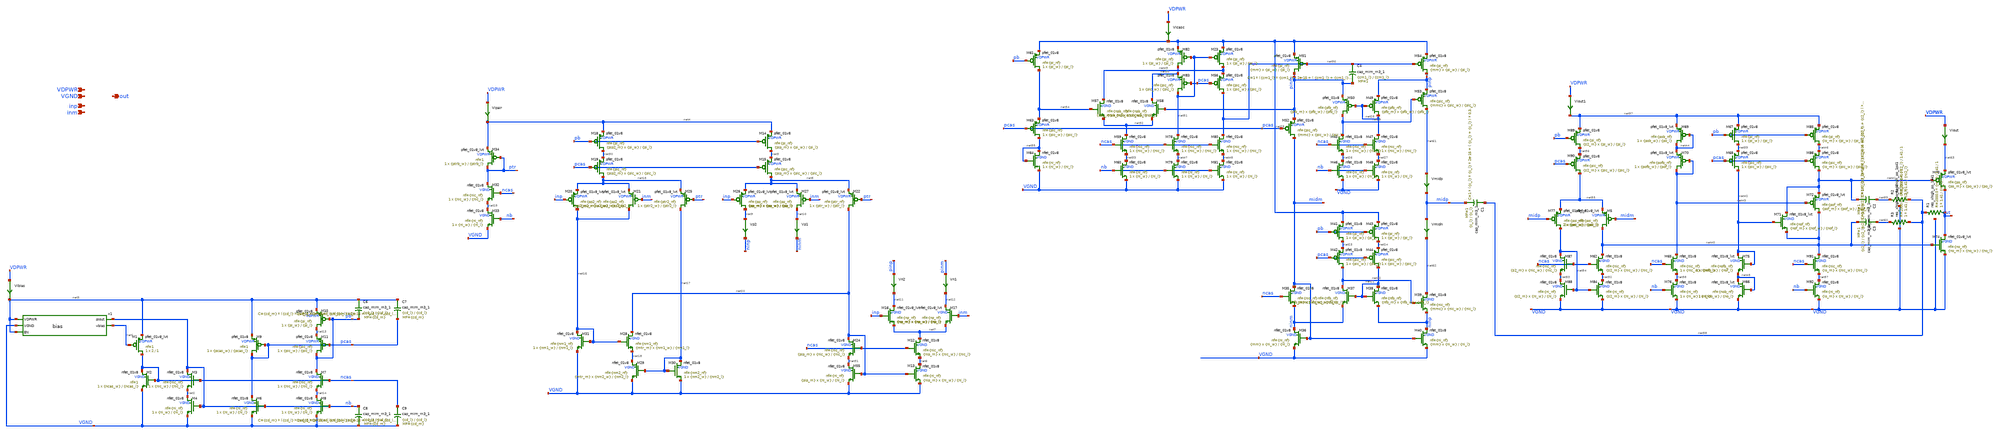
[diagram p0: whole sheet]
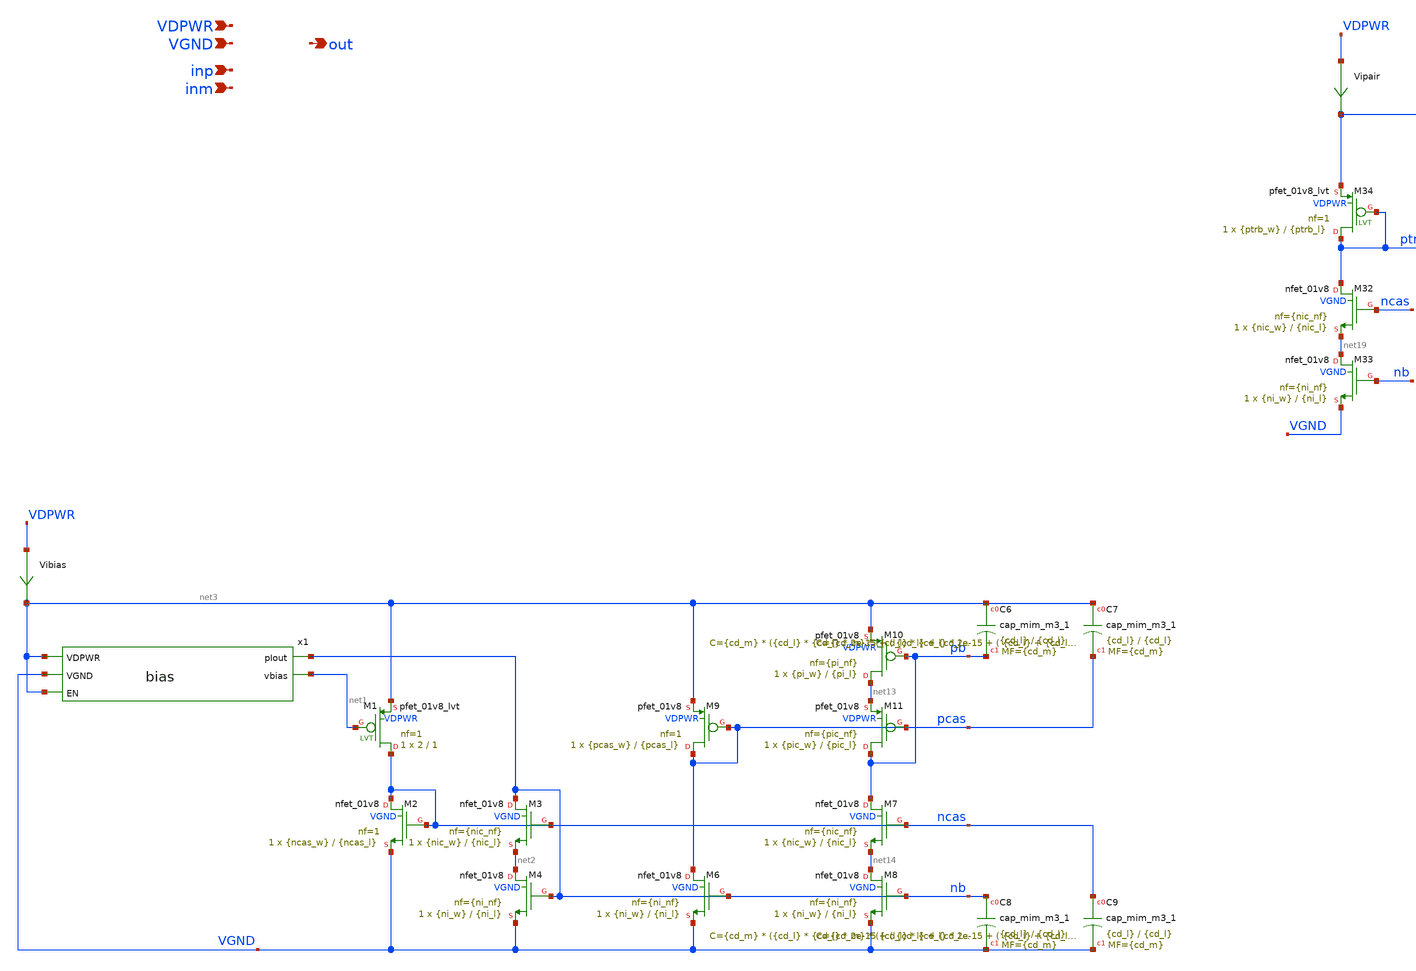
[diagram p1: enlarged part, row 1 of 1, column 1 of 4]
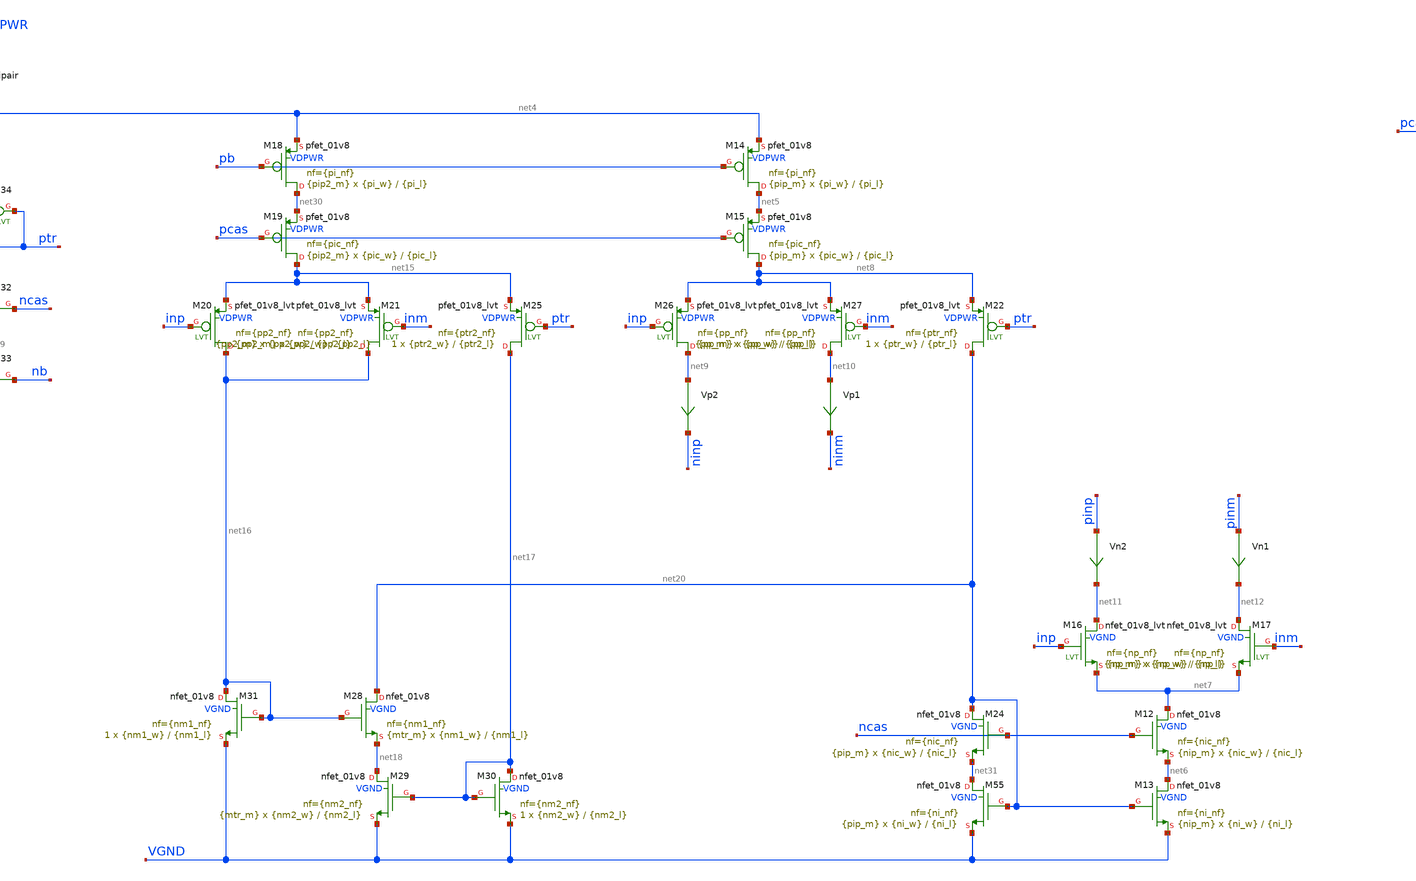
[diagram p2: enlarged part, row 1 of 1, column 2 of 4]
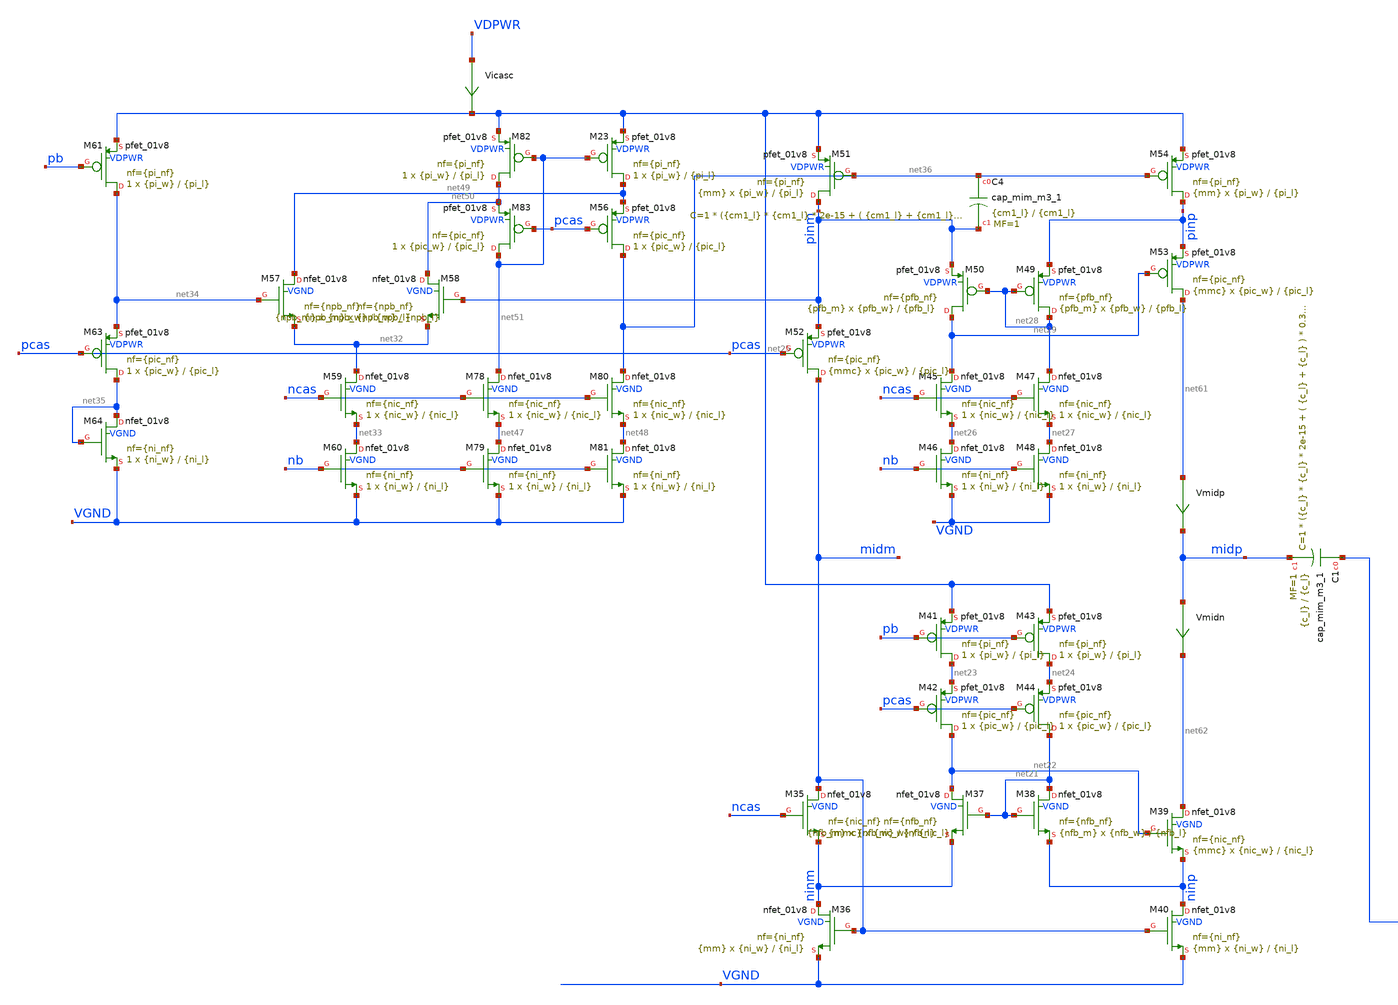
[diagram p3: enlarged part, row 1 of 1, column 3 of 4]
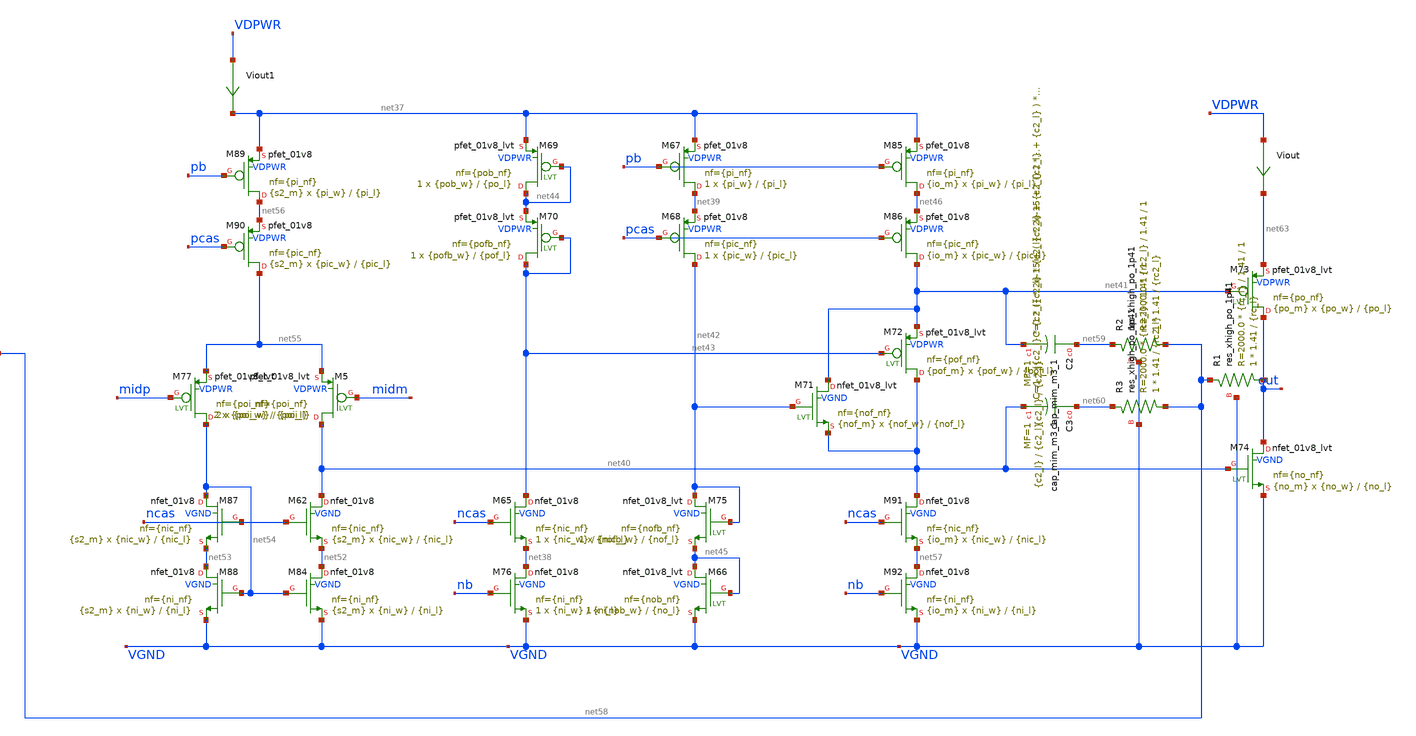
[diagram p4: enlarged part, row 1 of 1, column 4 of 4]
** sch_path: xschem/opamp_testing2.sch
**.subckt opamp_testing2 VDPWR VGND inp inm out
*.ipin VDPWR
*.ipin VGND
*.ipin inp
*.ipin inm
*.opin out
x1 net3 nb VGND net3 net1 bias
XM1 ncas net1 net3 VDPWR sky130_fd_pr__pfet_01v8_lvt L=1 W=2 nf=1 ad='int((1 + 1)/2) * 2 / 1 * 0.29'
+ as='int((1 + 2)/2) * 2 / 1 * 0.29' pd='2*int((1 + 1)/2) * (2 / 1 + 0.29)' ps='2*int((1 + 2)/2) * (2 / 1 + 0.29)'
+ nrd='0.29 / 2 ' nrs='0.29 / 2 ' sa=0 sb=0 sd=0 mult=1 m=1
XM2 ncas ncas VGND VGND sky130_fd_pr__nfet_01v8 L={ncas_l} W={ncas_w} nf=1 ad='int((1 + 1)/2) * {ncas_w} / 1 * 0.29'
+ as='int((1 + 2)/2) * {ncas_w} / 1 * 0.29' pd='2*int((1 + 1)/2) * ({ncas_w} / 1 + 0.29)' ps='2*int((1 + 2)/2) * ({ncas_w} / 1 + 0.29)'
+ nrd='0.29 / {ncas_w} ' nrs='0.29 / {ncas_w} ' sa=0 sb=0 sd=0 mult=1 m=1
XM3 nb ncas net2 VGND sky130_fd_pr__nfet_01v8 L={nic_l} W={nic_w} nf={nic_nf} ad='int(({nic_nf} + 1)/2) * {nic_w} / {nic_nf} * 0.29'
+ as='int(({nic_nf} + 2)/2) * {nic_w} / {nic_nf} * 0.29' pd='2*int(({nic_nf} + 1)/2) * ({nic_w} / {nic_nf} + 0.29)'
+ ps='2*int(({nic_nf} + 2)/2) * ({nic_w} / {nic_nf} + 0.29)' nrd='0.29 / {nic_w} ' nrs='0.29 / {nic_w} '
+ sa=0 sb=0 sd=0 mult=1 m=1
XM4 net2 nb VGND VGND sky130_fd_pr__nfet_01v8 L={ni_l} W={ni_w} nf={ni_nf} ad='int(({ni_nf} + 1)/2) * {ni_w} / {ni_nf} * 0.29'
+ as='int(({ni_nf} + 2)/2) * {ni_w} / {ni_nf} * 0.29' pd='2*int(({ni_nf} + 1)/2) * ({ni_w} / {ni_nf} + 0.29)'
+ ps='2*int(({ni_nf} + 2)/2) * ({ni_w} / {ni_nf} + 0.29)' nrd='0.29 / {ni_w} ' nrs='0.29 / {ni_w} ' sa=0
+ sb=0 sd=0 mult=1 m=1
XM6 pcas nb VGND VGND sky130_fd_pr__nfet_01v8 L={ni_l} W={ni_w} nf={ni_nf} ad='int(({ni_nf} + 1)/2) * {ni_w} / {ni_nf} * 0.29'
+ as='int(({ni_nf} + 2)/2) * {ni_w} / {ni_nf} * 0.29' pd='2*int(({ni_nf} + 1)/2) * ({ni_w} / {ni_nf} + 0.29)'
+ ps='2*int(({ni_nf} + 2)/2) * ({ni_w} / {ni_nf} + 0.29)' nrd='0.29 / {ni_w} ' nrs='0.29 / {ni_w} ' sa=0
+ sb=0 sd=0 mult=1 m=1
XM7 pb ncas net14 VGND sky130_fd_pr__nfet_01v8 L={nic_l} W={nic_w} nf={nic_nf} ad='int(({nic_nf} + 1)/2) * {nic_w} / {nic_nf} * 0.29'
+ as='int(({nic_nf} + 2)/2) * {nic_w} / {nic_nf} * 0.29' pd='2*int(({nic_nf} + 1)/2) * ({nic_w} / {nic_nf} + 0.29)'
+ ps='2*int(({nic_nf} + 2)/2) * ({nic_w} / {nic_nf} + 0.29)' nrd='0.29 / {nic_w} ' nrs='0.29 / {nic_w} '
+ sa=0 sb=0 sd=0 mult=1 m=1
XM8 net14 nb VGND VGND sky130_fd_pr__nfet_01v8 L={ni_l} W={ni_w} nf={ni_nf} ad='int(({ni_nf} + 1)/2) * {ni_w} / {ni_nf} * 0.29'
+ as='int(({ni_nf} + 2)/2) * {ni_w} / {ni_nf} * 0.29' pd='2*int(({ni_nf} + 1)/2) * ({ni_w} / {ni_nf} + 0.29)'
+ ps='2*int(({ni_nf} + 2)/2) * ({ni_w} / {ni_nf} + 0.29)' nrd='0.29 / {ni_w} ' nrs='0.29 / {ni_w} ' sa=0
+ sb=0 sd=0 mult=1 m=1
XM9 pcas pcas net3 VDPWR sky130_fd_pr__pfet_01v8 L={pcas_l} W={pcas_w} nf=1 ad='int((1 + 1)/2) * {pcas_w} / 1 * 0.29'
+ as='int((1 + 2)/2) * {pcas_w} / 1 * 0.29' pd='2*int((1 + 1)/2) * ({pcas_w} / 1 + 0.29)' ps='2*int((1 + 2)/2) * ({pcas_w} / 1 + 0.29)'
+ nrd='0.29 / {pcas_w} ' nrs='0.29 / {pcas_w} ' sa=0 sb=0 sd=0 mult=1 m=1
XM10 net13 pb net3 VDPWR sky130_fd_pr__pfet_01v8 L={pi_l} W={pi_w} nf={pi_nf} ad='int(({pi_nf} + 1)/2) * {pi_w} / {pi_nf} * 0.29'
+ as='int(({pi_nf} + 2)/2) * {pi_w} / {pi_nf} * 0.29' pd='2*int(({pi_nf} + 1)/2) * ({pi_w} / {pi_nf} + 0.29)'
+ ps='2*int(({pi_nf} + 2)/2) * ({pi_w} / {pi_nf} + 0.29)' nrd='0.29 / {pi_w} ' nrs='0.29 / {pi_w} ' sa=0
+ sb=0 sd=0 mult=1 m=1
XM11 pb pcas net13 VDPWR sky130_fd_pr__pfet_01v8 L={pic_l} W={pic_w} nf={pic_nf} ad='int(({pic_nf} + 1)/2) * {pic_w} / {pic_nf} * 0.29'
+ as='int(({pic_nf} + 2)/2) * {pic_w} / {pic_nf} * 0.29' pd='2*int(({pic_nf} + 1)/2) * ({pic_w} / {pic_nf} + 0.29)'
+ ps='2*int(({pic_nf} + 2)/2) * ({pic_w} / {pic_nf} + 0.29)' nrd='0.29 / {pic_w} ' nrs='0.29 / {pic_w} '
+ sa=0 sb=0 sd=0 mult=1 m=1
XM12 net7 ncas net6 VGND sky130_fd_pr__nfet_01v8 L={nic_l} W={nic_w} nf={nic_nf} ad='int(({nic_nf} + 1)/2) * {nic_w} / {nic_nf} * 0.29'
+ as='int(({nic_nf} + 2)/2) * {nic_w} / {nic_nf} * 0.29' pd='2*int(({nic_nf} + 1)/2) * ({nic_w} / {nic_nf} + 0.29)'
+ ps='2*int(({nic_nf} + 2)/2) * ({nic_w} / {nic_nf} + 0.29)' nrd='0.29 / {nic_w} ' nrs='0.29 / {nic_w} '
+ sa=0 sb=0 sd=0 mult={nip_m} m={nip_m}
XM13 net6 net20 VGND VGND sky130_fd_pr__nfet_01v8 L={ni_l} W={ni_w} nf={ni_nf} ad='int(({ni_nf} + 1)/2) * {ni_w} / {ni_nf} * 0.29'
+ as='int(({ni_nf} + 2)/2) * {ni_w} / {ni_nf} * 0.29' pd='2*int(({ni_nf} + 1)/2) * ({ni_w} / {ni_nf} + 0.29)'
+ ps='2*int(({ni_nf} + 2)/2) * ({ni_w} / {ni_nf} + 0.29)' nrd='0.29 / {ni_w} ' nrs='0.29 / {ni_w} ' sa=0
+ sb=0 sd=0 mult={nip_m} m={nip_m}
XM14 net5 pb net4 VDPWR sky130_fd_pr__pfet_01v8 L={pi_l} W={pi_w} nf={pi_nf} ad='int(({pi_nf} + 1)/2) * {pi_w} / {pi_nf} * 0.29'
+ as='int(({pi_nf} + 2)/2) * {pi_w} / {pi_nf} * 0.29' pd='2*int(({pi_nf} + 1)/2) * ({pi_w} / {pi_nf} + 0.29)'
+ ps='2*int(({pi_nf} + 2)/2) * ({pi_w} / {pi_nf} + 0.29)' nrd='0.29 / {pi_w} ' nrs='0.29 / {pi_w} ' sa=0
+ sb=0 sd=0 mult={pip_m} m={pip_m}
XM15 net8 pcas net5 VDPWR sky130_fd_pr__pfet_01v8 L={pic_l} W={pic_w} nf={pic_nf} ad='int(({pic_nf} + 1)/2) * {pic_w} / {pic_nf} * 0.29'
+ as='int(({pic_nf} + 2)/2) * {pic_w} / {pic_nf} * 0.29' pd='2*int(({pic_nf} + 1)/2) * ({pic_w} / {pic_nf} + 0.29)'
+ ps='2*int(({pic_nf} + 2)/2) * ({pic_w} / {pic_nf} + 0.29)' nrd='0.29 / {pic_w} ' nrs='0.29 / {pic_w} '
+ sa=0 sb=0 sd=0 mult={pip_m} m={pip_m}
XM16 net11 inp net7 VGND sky130_fd_pr__nfet_01v8_lvt L={np_l} W={np_w} nf={np_nf} ad='int(({np_nf} + 1)/2) * {np_w} / {np_nf} * 0.29'
+ as='int(({np_nf} + 2)/2) * {np_w} / {np_nf} * 0.29' pd='2*int(({np_nf} + 1)/2) * ({np_w} / {np_nf} + 0.29)'
+ ps='2*int(({np_nf} + 2)/2) * ({np_w} / {np_nf} + 0.29)' nrd='0.29 / {np_w} ' nrs='0.29 / {np_w} ' sa=0
+ sb=0 sd=0 mult={np_m} m={np_m}
XM17 net12 inm net7 VGND sky130_fd_pr__nfet_01v8_lvt L={np_l} W={np_w} nf={np_nf} ad='int(({np_nf} + 1)/2) * {np_w} / {np_nf} * 0.29'
+ as='int(({np_nf} + 2)/2) * {np_w} / {np_nf} * 0.29' pd='2*int(({np_nf} + 1)/2) * ({np_w} / {np_nf} + 0.29)'
+ ps='2*int(({np_nf} + 2)/2) * ({np_w} / {np_nf} + 0.29)' nrd='0.29 / {np_w} ' nrs='0.29 / {np_w} ' sa=0
+ sb=0 sd=0 mult={np_m} m={np_m}
XM26 net9 inp net8 VDPWR sky130_fd_pr__pfet_01v8_lvt L={pp_l} W={pp_w} nf={pp_nf} ad='int(({pp_nf} + 1)/2) * {pp_w} / {pp_nf} * 0.29'
+ as='int(({pp_nf} + 2)/2) * {pp_w} / {pp_nf} * 0.29' pd='2*int(({pp_nf} + 1)/2) * ({pp_w} / {pp_nf} + 0.29)'
+ ps='2*int(({pp_nf} + 2)/2) * ({pp_w} / {pp_nf} + 0.29)' nrd='0.29 / {pp_w} ' nrs='0.29 / {pp_w} ' sa=0
+ sb=0 sd=0 mult={pp_m} m={pp_m}
XM27 net10 inm net8 VDPWR sky130_fd_pr__pfet_01v8_lvt L={pp_l} W={pp_w} nf={pp_nf} ad='int(({pp_nf} + 1)/2) * {pp_w} / {pp_nf} * 0.29'
+ as='int(({pp_nf} + 2)/2) * {pp_w} / {pp_nf} * 0.29' pd='2*int(({pp_nf} + 1)/2) * ({pp_w} / {pp_nf} + 0.29)'
+ ps='2*int(({pp_nf} + 2)/2) * ({pp_w} / {pp_nf} + 0.29)' nrd='0.29 / {pp_w} ' nrs='0.29 / {pp_w} ' sa=0
+ sb=0 sd=0 mult={pp_m} m={pp_m}
Vp1 net10 ninm 0
.save i(vp1)
Vp2 net9 ninp 0
.save i(vp2)
Vn1 pinm net12 0
.save i(vn1)
Vn2 pinp net11 0
.save i(vn2)
XM18 net30 pb net4 VDPWR sky130_fd_pr__pfet_01v8 L={pi_l} W={pi_w} nf={pi_nf} ad='int(({pi_nf} + 1)/2) * {pi_w} / {pi_nf} * 0.29'
+ as='int(({pi_nf} + 2)/2) * {pi_w} / {pi_nf} * 0.29' pd='2*int(({pi_nf} + 1)/2) * ({pi_w} / {pi_nf} + 0.29)'
+ ps='2*int(({pi_nf} + 2)/2) * ({pi_w} / {pi_nf} + 0.29)' nrd='0.29 / {pi_w} ' nrs='0.29 / {pi_w} ' sa=0
+ sb=0 sd=0 mult={pip2_m} m={pip2_m}
XM19 net15 pcas net30 VDPWR sky130_fd_pr__pfet_01v8 L={pic_l} W={pic_w} nf={pic_nf} ad='int(({pic_nf} + 1)/2) * {pic_w} / {pic_nf} * 0.29'
+ as='int(({pic_nf} + 2)/2) * {pic_w} / {pic_nf} * 0.29' pd='2*int(({pic_nf} + 1)/2) * ({pic_w} / {pic_nf} + 0.29)'
+ ps='2*int(({pic_nf} + 2)/2) * ({pic_w} / {pic_nf} + 0.29)' nrd='0.29 / {pic_w} ' nrs='0.29 / {pic_w} '
+ sa=0 sb=0 sd=0 mult={pip2_m} m={pip2_m}
XM20 net16 inp net15 VDPWR sky130_fd_pr__pfet_01v8_lvt L={pp2_l} W={pp2_w} nf={pp2_nf} ad='int(({pp2_nf} + 1)/2) * {pp2_w} / {pp2_nf} * 0.29'
+ as='int(({pp2_nf} + 2)/2) * {pp2_w} / {pp2_nf} * 0.29' pd='2*int(({pp2_nf} + 1)/2) * ({pp2_w} / {pp2_nf} + 0.29)'
+ ps='2*int(({pp2_nf} + 2)/2) * ({pp2_w} / {pp2_nf} + 0.29)' nrd='0.29 / {pp2_w} ' nrs='0.29 / {pp2_w} '
+ sa=0 sb=0 sd=0 mult={pp2_m} m={pp2_m}
XM21 net16 inm net15 VDPWR sky130_fd_pr__pfet_01v8_lvt L={pp2_l} W={pp2_w} nf={pp2_nf} ad='int(({pp2_nf} + 1)/2) * {pp2_w} / {pp2_nf} * 0.29'
+ as='int(({pp2_nf} + 2)/2) * {pp2_w} / {pp2_nf} * 0.29' pd='2*int(({pp2_nf} + 1)/2) * ({pp2_w} / {pp2_nf} + 0.29)'
+ ps='2*int(({pp2_nf} + 2)/2) * ({pp2_w} / {pp2_nf} + 0.29)' nrd='0.29 / {pp2_w} ' nrs='0.29 / {pp2_w} '
+ sa=0 sb=0 sd=0 mult={pp2_m} m={pp2_m}
XM25 net17 ptr net15 VDPWR sky130_fd_pr__pfet_01v8_lvt L={ptr2_l} W={ptr2_w} nf={ptr2_nf} ad='int(({ptr2_nf} + 1)/2) * {ptr2_w} / {ptr2_nf} * 0.29'
+ as='int(({ptr2_nf} + 2)/2) * {ptr2_w} / {ptr2_nf} * 0.29' pd='2*int(({ptr2_nf} + 1)/2) * ({ptr2_w} / {ptr2_nf} + 0.29)'
+ ps='2*int(({ptr2_nf} + 2)/2) * ({ptr2_w} / {ptr2_nf} + 0.29)' nrd='0.29 / {ptr2_w} ' nrs='0.29 / {ptr2_w} '
+ sa=0 sb=0 sd=0 mult=1 m=1
XM28 net20 net16 net18 VGND sky130_fd_pr__nfet_01v8 L={nm1_l} W={nm1_w} nf={nm1_nf} ad='int(({nm1_nf} + 1)/2) * {nm1_w} / {nm1_nf} * 0.29'
+ as='int(({nm1_nf} + 2)/2) * {nm1_w} / {nm1_nf} * 0.29' pd='2*int(({nm1_nf} + 1)/2) * ({nm1_w} / {nm1_nf} + 0.29)'
+ ps='2*int(({nm1_nf} + 2)/2) * ({nm1_w} / {nm1_nf} + 0.29)' nrd='0.29 / {nm1_w} ' nrs='0.29 / {nm1_w} '
+ sa=0 sb=0 sd=0 mult={mtr_m} m={mtr_m}
XM29 net18 net17 VGND VGND sky130_fd_pr__nfet_01v8 L={nm2_l} W={nm2_w} nf={nm2_nf} ad='int(({nm2_nf} + 1)/2) * {nm2_w} / {nm2_nf} * 0.29'
+ as='int(({nm2_nf} + 2)/2) * {nm2_w} / {nm2_nf} * 0.29' pd='2*int(({nm2_nf} + 1)/2) * ({nm2_w} / {nm2_nf} + 0.29)'
+ ps='2*int(({nm2_nf} + 2)/2) * ({nm2_w} / {nm2_nf} + 0.29)' nrd='0.29 / {nm2_w} ' nrs='0.29 / {nm2_w} '
+ sa=0 sb=0 sd=0 mult={mtr_m} m={mtr_m}
XM30 net17 net17 VGND VGND sky130_fd_pr__nfet_01v8 L={nm2_l} W={nm2_w} nf={nm2_nf} ad='int(({nm2_nf} + 1)/2) * {nm2_w} / {nm2_nf} * 0.29'
+ as='int(({nm2_nf} + 2)/2) * {nm2_w} / {nm2_nf} * 0.29' pd='2*int(({nm2_nf} + 1)/2) * ({nm2_w} / {nm2_nf} + 0.29)'
+ ps='2*int(({nm2_nf} + 2)/2) * ({nm2_w} / {nm2_nf} + 0.29)' nrd='0.29 / {nm2_w} ' nrs='0.29 / {nm2_w} '
+ sa=0 sb=0 sd=0 mult=1 m=1
XM31 net16 net16 VGND VGND sky130_fd_pr__nfet_01v8 L={nm1_l} W={nm1_w} nf={nm1_nf} ad='int(({nm1_nf} + 1)/2) * {nm1_w} / {nm1_nf} * 0.29'
+ as='int(({nm1_nf} + 2)/2) * {nm1_w} / {nm1_nf} * 0.29' pd='2*int(({nm1_nf} + 1)/2) * ({nm1_w} / {nm1_nf} + 0.29)'
+ ps='2*int(({nm1_nf} + 2)/2) * ({nm1_w} / {nm1_nf} + 0.29)' nrd='0.29 / {nm1_w} ' nrs='0.29 / {nm1_w} '
+ sa=0 sb=0 sd=0 mult=1 m=1
XM32 ptr ncas net19 VGND sky130_fd_pr__nfet_01v8 L={nic_l} W={nic_w} nf={nic_nf} ad='int(({nic_nf} + 1)/2) * {nic_w} / {nic_nf} * 0.29'
+ as='int(({nic_nf} + 2)/2) * {nic_w} / {nic_nf} * 0.29' pd='2*int(({nic_nf} + 1)/2) * ({nic_w} / {nic_nf} + 0.29)'
+ ps='2*int(({nic_nf} + 2)/2) * ({nic_w} / {nic_nf} + 0.29)' nrd='0.29 / {nic_w} ' nrs='0.29 / {nic_w} '
+ sa=0 sb=0 sd=0 mult=1 m=1
XM33 net19 nb VGND VGND sky130_fd_pr__nfet_01v8 L={ni_l} W={ni_w} nf={ni_nf} ad='int(({ni_nf} + 1)/2) * {ni_w} / {ni_nf} * 0.29'
+ as='int(({ni_nf} + 2)/2) * {ni_w} / {ni_nf} * 0.29' pd='2*int(({ni_nf} + 1)/2) * ({ni_w} / {ni_nf} + 0.29)'
+ ps='2*int(({ni_nf} + 2)/2) * ({ni_w} / {ni_nf} + 0.29)' nrd='0.29 / {ni_w} ' nrs='0.29 / {ni_w} ' sa=0
+ sb=0 sd=0 mult=1 m=1
XM34 ptr ptr net4 VDPWR sky130_fd_pr__pfet_01v8_lvt L={ptrb_l} W={ptrb_w} nf=1 ad='int((1 + 1)/2) * {ptrb_w} / 1 * 0.29'
+ as='int((1 + 2)/2) * {ptrb_w} / 1 * 0.29' pd='2*int((1 + 1)/2) * ({ptrb_w} / 1 + 0.29)' ps='2*int((1 + 2)/2) * ({ptrb_w} / 1 + 0.29)'
+ nrd='0.29 / {ptrb_w} ' nrs='0.29 / {ptrb_w} ' sa=0 sb=0 sd=0 mult=1 m=1
XM35 midm ncas ninm VGND sky130_fd_pr__nfet_01v8 L={nic_l} W={nic_w} nf={nic_nf} ad='int(({nic_nf} + 1)/2) * {nic_w} / {nic_nf} * 0.29'
+ as='int(({nic_nf} + 2)/2) * {nic_w} / {nic_nf} * 0.29' pd='2*int(({nic_nf} + 1)/2) * ({nic_w} / {nic_nf} + 0.29)'
+ ps='2*int(({nic_nf} + 2)/2) * ({nic_w} / {nic_nf} + 0.29)' nrd='0.29 / {nic_w} ' nrs='0.29 / {nic_w} '
+ sa=0 sb=0 sd=0 mult={mmc} m={mmc}
XM36 ninm midm VGND VGND sky130_fd_pr__nfet_01v8 L={ni_l} W={ni_w} nf={ni_nf} ad='int(({ni_nf} + 1)/2) * {ni_w} / {ni_nf} * 0.29'
+ as='int(({ni_nf} + 2)/2) * {ni_w} / {ni_nf} * 0.29' pd='2*int(({ni_nf} + 1)/2) * ({ni_w} / {ni_nf} + 0.29)'
+ ps='2*int(({ni_nf} + 2)/2) * ({ni_w} / {ni_nf} + 0.29)' nrd='0.29 / {ni_w} ' nrs='0.29 / {ni_w} ' sa=0
+ sb=0 sd=0 mult={mm} m={mm}
XM37 net22 net21 ninm VGND sky130_fd_pr__nfet_01v8 L={nfb_l} W={nfb_w} nf={nfb_nf} ad='int(({nfb_nf} + 1)/2) * {nfb_w} / {nfb_nf} * 0.29'
+ as='int(({nfb_nf} + 2)/2) * {nfb_w} / {nfb_nf} * 0.29' pd='2*int(({nfb_nf} + 1)/2) * ({nfb_w} / {nfb_nf} + 0.29)'
+ ps='2*int(({nfb_nf} + 2)/2) * ({nfb_w} / {nfb_nf} + 0.29)' nrd='0.29 / {nfb_w} ' nrs='0.29 / {nfb_w} '
+ sa=0 sb=0 sd=0 mult={nfb_m} m={nfb_m}
XM39 net62 net22 ninp VGND sky130_fd_pr__nfet_01v8 L={nic_l} W={nic_w} nf={nic_nf} ad='int(({nic_nf} + 1)/2) * {nic_w} / {nic_nf} * 0.29'
+ as='int(({nic_nf} + 2)/2) * {nic_w} / {nic_nf} * 0.29' pd='2*int(({nic_nf} + 1)/2) * ({nic_w} / {nic_nf} + 0.29)'
+ ps='2*int(({nic_nf} + 2)/2) * ({nic_w} / {nic_nf} + 0.29)' nrd='0.29 / {nic_w} ' nrs='0.29 / {nic_w} '
+ sa=0 sb=0 sd=0 mult={mmc} m={mmc}
XM40 ninp midm VGND VGND sky130_fd_pr__nfet_01v8 L={ni_l} W={ni_w} nf={ni_nf} ad='int(({ni_nf} + 1)/2) * {ni_w} / {ni_nf} * 0.29'
+ as='int(({ni_nf} + 2)/2) * {ni_w} / {ni_nf} * 0.29' pd='2*int(({ni_nf} + 1)/2) * ({ni_w} / {ni_nf} + 0.29)'
+ ps='2*int(({ni_nf} + 2)/2) * ({ni_w} / {ni_nf} + 0.29)' nrd='0.29 / {ni_w} ' nrs='0.29 / {ni_w} ' sa=0
+ sb=0 sd=0 mult={mm} m={mm}
XM41 net23 pb net25 VDPWR sky130_fd_pr__pfet_01v8 L={pi_l} W={pi_w} nf={pi_nf} ad='int(({pi_nf} + 1)/2) * {pi_w} / {pi_nf} * 0.29'
+ as='int(({pi_nf} + 2)/2) * {pi_w} / {pi_nf} * 0.29' pd='2*int(({pi_nf} + 1)/2) * ({pi_w} / {pi_nf} + 0.29)'
+ ps='2*int(({pi_nf} + 2)/2) * ({pi_w} / {pi_nf} + 0.29)' nrd='0.29 / {pi_w} ' nrs='0.29 / {pi_w} ' sa=0
+ sb=0 sd=0 mult=1 m=1
XM42 net22 pcas net23 VDPWR sky130_fd_pr__pfet_01v8 L={pic_l} W={pic_w} nf={pic_nf} ad='int(({pic_nf} + 1)/2) * {pic_w} / {pic_nf} * 0.29'
+ as='int(({pic_nf} + 2)/2) * {pic_w} / {pic_nf} * 0.29' pd='2*int(({pic_nf} + 1)/2) * ({pic_w} / {pic_nf} + 0.29)'
+ ps='2*int(({pic_nf} + 2)/2) * ({pic_w} / {pic_nf} + 0.29)' nrd='0.29 / {pic_w} ' nrs='0.29 / {pic_w} '
+ sa=0 sb=0 sd=0 mult=1 m=1
XM43 net24 pb net25 VDPWR sky130_fd_pr__pfet_01v8 L={pi_l} W={pi_w} nf={pi_nf} ad='int(({pi_nf} + 1)/2) * {pi_w} / {pi_nf} * 0.29'
+ as='int(({pi_nf} + 2)/2) * {pi_w} / {pi_nf} * 0.29' pd='2*int(({pi_nf} + 1)/2) * ({pi_w} / {pi_nf} + 0.29)'
+ ps='2*int(({pi_nf} + 2)/2) * ({pi_w} / {pi_nf} + 0.29)' nrd='0.29 / {pi_w} ' nrs='0.29 / {pi_w} ' sa=0
+ sb=0 sd=0 mult=1 m=1
XM44 net21 pcas net24 VDPWR sky130_fd_pr__pfet_01v8 L={pic_l} W={pic_w} nf={pic_nf} ad='int(({pic_nf} + 1)/2) * {pic_w} / {pic_nf} * 0.29'
+ as='int(({pic_nf} + 2)/2) * {pic_w} / {pic_nf} * 0.29' pd='2*int(({pic_nf} + 1)/2) * ({pic_w} / {pic_nf} + 0.29)'
+ ps='2*int(({pic_nf} + 2)/2) * ({pic_w} / {pic_nf} + 0.29)' nrd='0.29 / {pic_w} ' nrs='0.29 / {pic_w} '
+ sa=0 sb=0 sd=0 mult=1 m=1
XM45 net29 ncas net26 VGND sky130_fd_pr__nfet_01v8 L={nic_l} W={nic_w} nf={nic_nf} ad='int(({nic_nf} + 1)/2) * {nic_w} / {nic_nf} * 0.29'
+ as='int(({nic_nf} + 2)/2) * {nic_w} / {nic_nf} * 0.29' pd='2*int(({nic_nf} + 1)/2) * ({nic_w} / {nic_nf} + 0.29)'
+ ps='2*int(({nic_nf} + 2)/2) * ({nic_w} / {nic_nf} + 0.29)' nrd='0.29 / {nic_w} ' nrs='0.29 / {nic_w} '
+ sa=0 sb=0 sd=0 mult=1 m=1
XM46 net26 nb VGND VGND sky130_fd_pr__nfet_01v8 L={ni_l} W={ni_w} nf={ni_nf} ad='int(({ni_nf} + 1)/2) * {ni_w} / {ni_nf} * 0.29'
+ as='int(({ni_nf} + 2)/2) * {ni_w} / {ni_nf} * 0.29' pd='2*int(({ni_nf} + 1)/2) * ({ni_w} / {ni_nf} + 0.29)'
+ ps='2*int(({ni_nf} + 2)/2) * ({ni_w} / {ni_nf} + 0.29)' nrd='0.29 / {ni_w} ' nrs='0.29 / {ni_w} ' sa=0
+ sb=0 sd=0 mult=1 m=1
XM47 net28 ncas net27 VGND sky130_fd_pr__nfet_01v8 L={nic_l} W={nic_w} nf={nic_nf} ad='int(({nic_nf} + 1)/2) * {nic_w} / {nic_nf} * 0.29'
+ as='int(({nic_nf} + 2)/2) * {nic_w} / {nic_nf} * 0.29' pd='2*int(({nic_nf} + 1)/2) * ({nic_w} / {nic_nf} + 0.29)'
+ ps='2*int(({nic_nf} + 2)/2) * ({nic_w} / {nic_nf} + 0.29)' nrd='0.29 / {nic_w} ' nrs='0.29 / {nic_w} '
+ sa=0 sb=0 sd=0 mult=1 m=1
XM48 net27 nb VGND VGND sky130_fd_pr__nfet_01v8 L={ni_l} W={ni_w} nf={ni_nf} ad='int(({ni_nf} + 1)/2) * {ni_w} / {ni_nf} * 0.29'
+ as='int(({ni_nf} + 2)/2) * {ni_w} / {ni_nf} * 0.29' pd='2*int(({ni_nf} + 1)/2) * ({ni_w} / {ni_nf} + 0.29)'
+ ps='2*int(({ni_nf} + 2)/2) * ({ni_w} / {ni_nf} + 0.29)' nrd='0.29 / {ni_w} ' nrs='0.29 / {ni_w} ' sa=0
+ sb=0 sd=0 mult=1 m=1
XM50 net29 net28 pinm VDPWR sky130_fd_pr__pfet_01v8 L={pfb_l} W={pfb_w} nf={pfb_nf} ad='int(({pfb_nf} + 1)/2) * {pfb_w} / {pfb_nf} * 0.29'
+ as='int(({pfb_nf} + 2)/2) * {pfb_w} / {pfb_nf} * 0.29' pd='2*int(({pfb_nf} + 1)/2) * ({pfb_w} / {pfb_nf} + 0.29)'
+ ps='2*int(({pfb_nf} + 2)/2) * ({pfb_w} / {pfb_nf} + 0.29)' nrd='0.29 / {pfb_w} ' nrs='0.29 / {pfb_w} '
+ sa=0 sb=0 sd=0 mult={pfb_m} m={pfb_m}
XM51 pinm net36 net25 VDPWR sky130_fd_pr__pfet_01v8 L={pi_l} W={pi_w} nf={pi_nf} ad='int(({pi_nf} + 1)/2) * {pi_w} / {pi_nf} * 0.29'
+ as='int(({pi_nf} + 2)/2) * {pi_w} / {pi_nf} * 0.29' pd='2*int(({pi_nf} + 1)/2) * ({pi_w} / {pi_nf} + 0.29)'
+ ps='2*int(({pi_nf} + 2)/2) * ({pi_w} / {pi_nf} + 0.29)' nrd='0.29 / {pi_w} ' nrs='0.29 / {pi_w} ' sa=0
+ sb=0 sd=0 mult={mm} m={mm}
XM52 midm pcas pinm VDPWR sky130_fd_pr__pfet_01v8 L={pic_l} W={pic_w} nf={pic_nf} ad='int(({pic_nf} + 1)/2) * {pic_w} / {pic_nf} * 0.29'
+ as='int(({pic_nf} + 2)/2) * {pic_w} / {pic_nf} * 0.29' pd='2*int(({pic_nf} + 1)/2) * ({pic_w} / {pic_nf} + 0.29)'
+ ps='2*int(({pic_nf} + 2)/2) * ({pic_w} / {pic_nf} + 0.29)' nrd='0.29 / {pic_w} ' nrs='0.29 / {pic_w} '
+ sa=0 sb=0 sd=0 mult={mmc} m={mmc}
XM53 net61 net29 pinp VDPWR sky130_fd_pr__pfet_01v8 L={pic_l} W={pic_w} nf={pic_nf} ad='int(({pic_nf} + 1)/2) * {pic_w} / {pic_nf} * 0.29'
+ as='int(({pic_nf} + 2)/2) * {pic_w} / {pic_nf} * 0.29' pd='2*int(({pic_nf} + 1)/2) * ({pic_w} / {pic_nf} + 0.29)'
+ ps='2*int(({pic_nf} + 2)/2) * ({pic_w} / {pic_nf} + 0.29)' nrd='0.29 / {pic_w} ' nrs='0.29 / {pic_w} '
+ sa=0 sb=0 sd=0 mult={mmc} m={mmc}
XM54 pinp net36 net25 VDPWR sky130_fd_pr__pfet_01v8 L={pi_l} W={pi_w} nf={pi_nf} ad='int(({pi_nf} + 1)/2) * {pi_w} / {pi_nf} * 0.29'
+ as='int(({pi_nf} + 2)/2) * {pi_w} / {pi_nf} * 0.29' pd='2*int(({pi_nf} + 1)/2) * ({pi_w} / {pi_nf} + 0.29)'
+ ps='2*int(({pi_nf} + 2)/2) * ({pi_w} / {pi_nf} + 0.29)' nrd='0.29 / {pi_w} ' nrs='0.29 / {pi_w} ' sa=0
+ sb=0 sd=0 mult={mm} m={mm}
Vibias VDPWR net3 0
.save i(vibias)
Vipair VDPWR net4 0
.save i(vipair)
Vicasc VDPWR net25 0
.save i(vicasc)
XM49 net28 net28 pinp VDPWR sky130_fd_pr__pfet_01v8 L={pfb_l} W={pfb_w} nf={pfb_nf} ad='int(({pfb_nf} + 1)/2) * {pfb_w} / {pfb_nf} * 0.29'
+ as='int(({pfb_nf} + 2)/2) * {pfb_w} / {pfb_nf} * 0.29' pd='2*int(({pfb_nf} + 1)/2) * ({pfb_w} / {pfb_nf} + 0.29)'
+ ps='2*int(({pfb_nf} + 2)/2) * ({pfb_w} / {pfb_nf} + 0.29)' nrd='0.29 / {pfb_w} ' nrs='0.29 / {pfb_w} '
+ sa=0 sb=0 sd=0 mult={pfb_m} m={pfb_m}
XM38 net21 net21 ninp VGND sky130_fd_pr__nfet_01v8 L={nfb_l} W={nfb_w} nf={nfb_nf} ad='int(({nfb_nf} + 1)/2) * {nfb_w} / {nfb_nf} * 0.29'
+ as='int(({nfb_nf} + 2)/2) * {nfb_w} / {nfb_nf} * 0.29' pd='2*int(({nfb_nf} + 1)/2) * ({nfb_w} / {nfb_nf} + 0.29)'
+ ps='2*int(({nfb_nf} + 2)/2) * ({nfb_w} / {nfb_nf} + 0.29)' nrd='0.29 / {nfb_w} ' nrs='0.29 / {nfb_w} '
+ sa=0 sb=0 sd=0 mult={nfb_m} m={nfb_m}
XM24 net20 ncas net31 VGND sky130_fd_pr__nfet_01v8 L={nic_l} W={nic_w} nf={nic_nf} ad='int(({nic_nf} + 1)/2) * {nic_w} / {nic_nf} * 0.29'
+ as='int(({nic_nf} + 2)/2) * {nic_w} / {nic_nf} * 0.29' pd='2*int(({nic_nf} + 1)/2) * ({nic_w} / {nic_nf} + 0.29)'
+ ps='2*int(({nic_nf} + 2)/2) * ({nic_w} / {nic_nf} + 0.29)' nrd='0.29 / {nic_w} ' nrs='0.29 / {nic_w} '
+ sa=0 sb=0 sd=0 mult={pip_m} m={pip_m}
XM55 net31 net20 VGND VGND sky130_fd_pr__nfet_01v8 L={ni_l} W={ni_w} nf={ni_nf} ad='int(({ni_nf} + 1)/2) * {ni_w} / {ni_nf} * 0.29'
+ as='int(({ni_nf} + 2)/2) * {ni_w} / {ni_nf} * 0.29' pd='2*int(({ni_nf} + 1)/2) * ({ni_w} / {ni_nf} + 0.29)'
+ ps='2*int(({ni_nf} + 2)/2) * ({ni_w} / {ni_nf} + 0.29)' nrd='0.29 / {ni_w} ' nrs='0.29 / {ni_w} ' sa=0
+ sb=0 sd=0 mult={pip_m} m={pip_m}
XM22 net20 ptr net8 VDPWR sky130_fd_pr__pfet_01v8_lvt L={ptr_l} W={ptr_w} nf={ptr_nf} ad='int(({ptr_nf} + 1)/2) * {ptr_w} / {ptr_nf} * 0.29'
+ as='int(({ptr_nf} + 2)/2) * {ptr_w} / {ptr_nf} * 0.29' pd='2*int(({ptr_nf} + 1)/2) * ({ptr_w} / {ptr_nf} + 0.29)'
+ ps='2*int(({ptr_nf} + 2)/2) * ({ptr_w} / {ptr_nf} + 0.29)' nrd='0.29 / {ptr_w} ' nrs='0.29 / {ptr_w} '
+ sa=0 sb=0 sd=0 mult=1 m=1
XM57 net49 net34 net32 VGND sky130_fd_pr__nfet_01v8 L={npb_l} W={npb_w} nf={npb_nf} ad='int(({npb_nf} + 1)/2) * {npb_w} / {npb_nf} * 0.29'
+ as='int(({npb_nf} + 2)/2) * {npb_w} / {npb_nf} * 0.29' pd='2*int(({npb_nf} + 1)/2) * ({npb_w} / {npb_nf} + 0.29)'
+ ps='2*int(({npb_nf} + 2)/2) * ({npb_w} / {npb_nf} + 0.29)' nrd='0.29 / {npb_w} ' nrs='0.29 / {npb_w} '
+ sa=0 sb=0 sd=0 mult={npb_m} m={npb_m}
XM58 net50 pinm net32 VGND sky130_fd_pr__nfet_01v8 L={npb_l} W={npb_w} nf={npb_nf} ad='int(({npb_nf} + 1)/2) * {npb_w} / {npb_nf} * 0.29'
+ as='int(({npb_nf} + 2)/2) * {npb_w} / {npb_nf} * 0.29' pd='2*int(({npb_nf} + 1)/2) * ({npb_w} / {npb_nf} + 0.29)'
+ ps='2*int(({npb_nf} + 2)/2) * ({npb_w} / {npb_nf} + 0.29)' nrd='0.29 / {npb_w} ' nrs='0.29 / {npb_w} '
+ sa=0 sb=0 sd=0 mult={npb_m} m={npb_m}
XM59 net32 ncas net33 VGND sky130_fd_pr__nfet_01v8 L={nic_l} W={nic_w} nf={nic_nf} ad='int(({nic_nf} + 1)/2) * {nic_w} / {nic_nf} * 0.29'
+ as='int(({nic_nf} + 2)/2) * {nic_w} / {nic_nf} * 0.29' pd='2*int(({nic_nf} + 1)/2) * ({nic_w} / {nic_nf} + 0.29)'
+ ps='2*int(({nic_nf} + 2)/2) * ({nic_w} / {nic_nf} + 0.29)' nrd='0.29 / {nic_w} ' nrs='0.29 / {nic_w} '
+ sa=0 sb=0 sd=0 mult=1 m=1
XM60 net33 nb VGND VGND sky130_fd_pr__nfet_01v8 L={ni_l} W={ni_w} nf={ni_nf} ad='int(({ni_nf} + 1)/2) * {ni_w} / {ni_nf} * 0.29'
+ as='int(({ni_nf} + 2)/2) * {ni_w} / {ni_nf} * 0.29' pd='2*int(({ni_nf} + 1)/2) * ({ni_w} / {ni_nf} + 0.29)'
+ ps='2*int(({ni_nf} + 2)/2) * ({ni_w} / {ni_nf} + 0.29)' nrd='0.29 / {ni_w} ' nrs='0.29 / {ni_w} ' sa=0
+ sb=0 sd=0 mult=1 m=1
XM61 net34 pb net25 VDPWR sky130_fd_pr__pfet_01v8 L={pi_l} W={pi_w} nf={pi_nf} ad='int(({pi_nf} + 1)/2) * {pi_w} / {pi_nf} * 0.29'
+ as='int(({pi_nf} + 2)/2) * {pi_w} / {pi_nf} * 0.29' pd='2*int(({pi_nf} + 1)/2) * ({pi_w} / {pi_nf} + 0.29)'
+ ps='2*int(({pi_nf} + 2)/2) * ({pi_w} / {pi_nf} + 0.29)' nrd='0.29 / {pi_w} ' nrs='0.29 / {pi_w} ' sa=0
+ sb=0 sd=0 mult=1 m=1
XM63 net35 pcas net34 VDPWR sky130_fd_pr__pfet_01v8 L={pic_l} W={pic_w} nf={pic_nf} ad='int(({pic_nf} + 1)/2) * {pic_w} / {pic_nf} * 0.29'
+ as='int(({pic_nf} + 2)/2) * {pic_w} / {pic_nf} * 0.29' pd='2*int(({pic_nf} + 1)/2) * ({pic_w} / {pic_nf} + 0.29)'
+ ps='2*int(({pic_nf} + 2)/2) * ({pic_w} / {pic_nf} + 0.29)' nrd='0.29 / {pic_w} ' nrs='0.29 / {pic_w} '
+ sa=0 sb=0 sd=0 mult=1 m=1
XM64 net35 net35 VGND VGND sky130_fd_pr__nfet_01v8 L={ni_l} W={ni_w} nf={ni_nf} ad='int(({ni_nf} + 1)/2) * {ni_w} / {ni_nf} * 0.29'
+ as='int(({ni_nf} + 2)/2) * {ni_w} / {ni_nf} * 0.29' pd='2*int(({ni_nf} + 1)/2) * ({ni_w} / {ni_nf} + 0.29)'
+ ps='2*int(({ni_nf} + 2)/2) * ({ni_w} / {ni_nf} + 0.29)' nrd='0.29 / {ni_w} ' nrs='0.29 / {ni_w} ' sa=0
+ sb=0 sd=0 mult=1 m=1
XM65 net43 ncas net38 VGND sky130_fd_pr__nfet_01v8 L={nic_l} W={nic_w} nf={nic_nf} ad='int(({nic_nf} + 1)/2) * {nic_w} / {nic_nf} * 0.29'
+ as='int(({nic_nf} + 2)/2) * {nic_w} / {nic_nf} * 0.29' pd='2*int(({nic_nf} + 1)/2) * ({nic_w} / {nic_nf} + 0.29)'
+ ps='2*int(({nic_nf} + 2)/2) * ({nic_w} / {nic_nf} + 0.29)' nrd='0.29 / {nic_w} ' nrs='0.29 / {nic_w} '
+ sa=0 sb=0 sd=0 mult=1 m=1
XM66 net45 net45 VGND VGND sky130_fd_pr__nfet_01v8_lvt L={no_l} W={nob_w} nf={nob_nf} ad='int(({nob_nf} + 1)/2) * {nob_w} / {nob_nf} * 0.29'
+ as='int(({nob_nf} + 2)/2) * {nob_w} / {nob_nf} * 0.29' pd='2*int(({nob_nf} + 1)/2) * ({nob_w} / {nob_nf} + 0.29)'
+ ps='2*int(({nob_nf} + 2)/2) * ({nob_w} / {nob_nf} + 0.29)' nrd='0.29 / {nob_w} ' nrs='0.29 / {nob_w} '
+ sa=0 sb=0 sd=0 mult=1 m=1
XM67 net39 pb net37 VDPWR sky130_fd_pr__pfet_01v8 L={pi_l} W={pi_w} nf={pi_nf} ad='int(({pi_nf} + 1)/2) * {pi_w} / {pi_nf} * 0.29'
+ as='int(({pi_nf} + 2)/2) * {pi_w} / {pi_nf} * 0.29' pd='2*int(({pi_nf} + 1)/2) * ({pi_w} / {pi_nf} + 0.29)'
+ ps='2*int(({pi_nf} + 2)/2) * ({pi_w} / {pi_nf} + 0.29)' nrd='0.29 / {pi_w} ' nrs='0.29 / {pi_w} ' sa=0
+ sb=0 sd=0 mult=1 m=1
XM68 net42 pcas net39 VDPWR sky130_fd_pr__pfet_01v8 L={pic_l} W={pic_w} nf={pic_nf} ad='int(({pic_nf} + 1)/2) * {pic_w} / {pic_nf} * 0.29'
+ as='int(({pic_nf} + 2)/2) * {pic_w} / {pic_nf} * 0.29' pd='2*int(({pic_nf} + 1)/2) * ({pic_w} / {pic_nf} + 0.29)'
+ ps='2*int(({pic_nf} + 2)/2) * ({pic_w} / {pic_nf} + 0.29)' nrd='0.29 / {pic_w} ' nrs='0.29 / {pic_w} '
+ sa=0 sb=0 sd=0 mult=1 m=1
XM69 net44 net44 net37 VDPWR sky130_fd_pr__pfet_01v8_lvt L={po_l} W={pob_w} nf={pob_nf} ad='int(({pob_nf} + 1)/2) * {pob_w} / {pob_nf} * 0.29'
+ as='int(({pob_nf} + 2)/2) * {pob_w} / {pob_nf} * 0.29' pd='2*int(({pob_nf} + 1)/2) * ({pob_w} / {pob_nf} + 0.29)'
+ ps='2*int(({pob_nf} + 2)/2) * ({pob_w} / {pob_nf} + 0.29)' nrd='0.29 / {pob_w} ' nrs='0.29 / {pob_w} '
+ sa=0 sb=0 sd=0 mult=1 m=1
XM70 net43 net43 net44 VDPWR sky130_fd_pr__pfet_01v8_lvt L={pof_l} W={pofb_w} nf={pofb_nf} ad='int(({pofb_nf} + 1)/2) * {pofb_w} / {pofb_nf} * 0.29'
+ as='int(({pofb_nf} + 2)/2) * {pofb_w} / {pofb_nf} * 0.29' pd='2*int(({pofb_nf} + 1)/2) * ({pofb_w} / {pofb_nf} + 0.29)'
+ ps='2*int(({pofb_nf} + 2)/2) * ({pofb_w} / {pofb_nf} + 0.29)' nrd='0.29 / {pofb_w} ' nrs='0.29 / {pofb_w} '
+ sa=0 sb=0 sd=0 mult=1 m=1
XM71 net41 net42 net40 VGND sky130_fd_pr__nfet_01v8_lvt L={nof_l} W={nof_w} nf={nof_nf} ad='int(({nof_nf} + 1)/2) * {nof_w} / {nof_nf} * 0.29'
+ as='int(({nof_nf} + 2)/2) * {nof_w} / {nof_nf} * 0.29' pd='2*int(({nof_nf} + 1)/2) * ({nof_w} / {nof_nf} + 0.29)'
+ ps='2*int(({nof_nf} + 2)/2) * ({nof_w} / {nof_nf} + 0.29)' nrd='0.29 / {nof_w} ' nrs='0.29 / {nof_w} '
+ sa=0 sb=0 sd=0 mult={nof_m} m={nof_m}
XM72 net40 net43 net41 VDPWR sky130_fd_pr__pfet_01v8_lvt L={pof_l} W={pof_w} nf={pof_nf} ad='int(({pof_nf} + 1)/2) * {pof_w} / {pof_nf} * 0.29'
+ as='int(({pof_nf} + 2)/2) * {pof_w} / {pof_nf} * 0.29' pd='2*int(({pof_nf} + 1)/2) * ({pof_w} / {pof_nf} + 0.29)'
+ ps='2*int(({pof_nf} + 2)/2) * ({pof_w} / {pof_nf} + 0.29)' nrd='0.29 / {pof_w} ' nrs='0.29 / {pof_w} '
+ sa=0 sb=0 sd=0 mult={pof_m} m={pof_m}
Viout VDPWR net63 0
.save i(viout)
XM73 out net41 net63 VDPWR sky130_fd_pr__pfet_01v8_lvt L={po_l} W={po_w} nf={po_nf} ad='int(({po_nf} + 1)/2) * {po_w} / {po_nf} * 0.29'
+ as='int(({po_nf} + 2)/2) * {po_w} / {po_nf} * 0.29' pd='2*int(({po_nf} + 1)/2) * ({po_w} / {po_nf} + 0.29)'
+ ps='2*int(({po_nf} + 2)/2) * ({po_w} / {po_nf} + 0.29)' nrd='0.29 / {po_w} ' nrs='0.29 / {po_w} ' sa=0
+ sb=0 sd=0 mult={po_m} m={po_m}
XM74 out net40 VGND VGND sky130_fd_pr__nfet_01v8_lvt L={no_l} W={no_w} nf={no_nf} ad='int(({no_nf} + 1)/2) * {no_w} / {no_nf} * 0.29'
+ as='int(({no_nf} + 2)/2) * {no_w} / {no_nf} * 0.29' pd='2*int(({no_nf} + 1)/2) * ({no_w} / {no_nf} + 0.29)'
+ ps='2*int(({no_nf} + 2)/2) * ({no_w} / {no_nf} + 0.29)' nrd='0.29 / {no_w} ' nrs='0.29 / {no_w} ' sa=0
+ sb=0 sd=0 mult={no_m} m={no_m}
XM75 net42 net42 net45 VGND sky130_fd_pr__nfet_01v8_lvt L={nof_l} W={nofb_w} nf={nofb_nf} ad='int(({nofb_nf} + 1)/2) * {nofb_w} / {nofb_nf} * 0.29'
+ as='int(({nofb_nf} + 2)/2) * {nofb_w} / {nofb_nf} * 0.29' pd='2*int(({nofb_nf} + 1)/2) * ({nofb_w} / {nofb_nf} + 0.29)'
+ ps='2*int(({nofb_nf} + 2)/2) * ({nofb_w} / {nofb_nf} + 0.29)' nrd='0.29 / {nofb_w} ' nrs='0.29 / {nofb_w} '
+ sa=0 sb=0 sd=0 mult=1 m=1
XM76 net38 nb VGND VGND sky130_fd_pr__nfet_01v8 L={ni_l} W={ni_w} nf={ni_nf} ad='int(({ni_nf} + 1)/2) * {ni_w} / {ni_nf} * 0.29'
+ as='int(({ni_nf} + 2)/2) * {ni_w} / {ni_nf} * 0.29' pd='2*int(({ni_nf} + 1)/2) * ({ni_w} / {ni_nf} + 0.29)'
+ ps='2*int(({ni_nf} + 2)/2) * ({ni_w} / {ni_nf} + 0.29)' nrd='0.29 / {ni_w} ' nrs='0.29 / {ni_w} ' sa=0
+ sb=0 sd=0 mult=1 m=1
XM85 net46 pb net37 VDPWR sky130_fd_pr__pfet_01v8 L={pi_l} W={pi_w} nf={pi_nf} ad='int(({pi_nf} + 1)/2) * {pi_w} / {pi_nf} * 0.29'
+ as='int(({pi_nf} + 2)/2) * {pi_w} / {pi_nf} * 0.29' pd='2*int(({pi_nf} + 1)/2) * ({pi_w} / {pi_nf} + 0.29)'
+ ps='2*int(({pi_nf} + 2)/2) * ({pi_w} / {pi_nf} + 0.29)' nrd='0.29 / {pi_w} ' nrs='0.29 / {pi_w} ' sa=0
+ sb=0 sd=0 mult={io_m} m={io_m}
XM86 net41 pcas net46 VDPWR sky130_fd_pr__pfet_01v8 L={pic_l} W={pic_w} nf={pic_nf} ad='int(({pic_nf} + 1)/2) * {pic_w} / {pic_nf} * 0.29'
+ as='int(({pic_nf} + 2)/2) * {pic_w} / {pic_nf} * 0.29' pd='2*int(({pic_nf} + 1)/2) * ({pic_w} / {pic_nf} + 0.29)'
+ ps='2*int(({pic_nf} + 2)/2) * ({pic_w} / {pic_nf} + 0.29)' nrd='0.29 / {pic_w} ' nrs='0.29 / {pic_w} '
+ sa=0 sb=0 sd=0 mult={io_m} m={io_m}
XM77 net54 midp net55 VDPWR sky130_fd_pr__pfet_01v8_lvt L={poi_l} W={poi_w} nf={poi_nf} ad='int(({poi_nf} + 1)/2) * {poi_w} / {poi_nf} * 0.29'
+ as='int(({poi_nf} + 2)/2) * {poi_w} / {poi_nf} * 0.29' pd='2*int(({poi_nf} + 1)/2) * ({poi_w} / {poi_nf} + 0.29)'
+ ps='2*int(({poi_nf} + 2)/2) * ({poi_w} / {poi_nf} + 0.29)' nrd='0.29 / {poi_w} ' nrs='0.29 / {poi_w} '
+ sa=0 sb=0 sd=0 mult=2 m=2
Viout1 VDPWR net37 0
.save i(viout1)
XM78 net51 ncas net47 VGND sky130_fd_pr__nfet_01v8 L={nic_l} W={nic_w} nf={nic_nf} ad='int(({nic_nf} + 1)/2) * {nic_w} / {nic_nf} * 0.29'
+ as='int(({nic_nf} + 2)/2) * {nic_w} / {nic_nf} * 0.29' pd='2*int(({nic_nf} + 1)/2) * ({nic_w} / {nic_nf} + 0.29)'
+ ps='2*int(({nic_nf} + 2)/2) * ({nic_w} / {nic_nf} + 0.29)' nrd='0.29 / {nic_w} ' nrs='0.29 / {nic_w} '
+ sa=0 sb=0 sd=0 mult=1 m=1
XM79 net47 nb VGND VGND sky130_fd_pr__nfet_01v8 L={ni_l} W={ni_w} nf={ni_nf} ad='int(({ni_nf} + 1)/2) * {ni_w} / {ni_nf} * 0.29'
+ as='int(({ni_nf} + 2)/2) * {ni_w} / {ni_nf} * 0.29' pd='2*int(({ni_nf} + 1)/2) * ({ni_w} / {ni_nf} + 0.29)'
+ ps='2*int(({ni_nf} + 2)/2) * ({ni_w} / {ni_nf} + 0.29)' nrd='0.29 / {ni_w} ' nrs='0.29 / {ni_w} ' sa=0
+ sb=0 sd=0 mult=1 m=1
XM80 net36 ncas net48 VGND sky130_fd_pr__nfet_01v8 L={nic_l} W={nic_w} nf={nic_nf} ad='int(({nic_nf} + 1)/2) * {nic_w} / {nic_nf} * 0.29'
+ as='int(({nic_nf} + 2)/2) * {nic_w} / {nic_nf} * 0.29' pd='2*int(({nic_nf} + 1)/2) * ({nic_w} / {nic_nf} + 0.29)'
+ ps='2*int(({nic_nf} + 2)/2) * ({nic_w} / {nic_nf} + 0.29)' nrd='0.29 / {nic_w} ' nrs='0.29 / {nic_w} '
+ sa=0 sb=0 sd=0 mult=1 m=1
XM81 net48 nb VGND VGND sky130_fd_pr__nfet_01v8 L={ni_l} W={ni_w} nf={ni_nf} ad='int(({ni_nf} + 1)/2) * {ni_w} / {ni_nf} * 0.29'
+ as='int(({ni_nf} + 2)/2) * {ni_w} / {ni_nf} * 0.29' pd='2*int(({ni_nf} + 1)/2) * ({ni_w} / {ni_nf} + 0.29)'
+ ps='2*int(({ni_nf} + 2)/2) * ({ni_w} / {ni_nf} + 0.29)' nrd='0.29 / {ni_w} ' nrs='0.29 / {ni_w} ' sa=0
+ sb=0 sd=0 mult=1 m=1
XM23 net49 net51 net25 VDPWR sky130_fd_pr__pfet_01v8 L={pi_l} W={pi_w} nf={pi_nf} ad='int(({pi_nf} + 1)/2) * {pi_w} / {pi_nf} * 0.29'
+ as='int(({pi_nf} + 2)/2) * {pi_w} / {pi_nf} * 0.29' pd='2*int(({pi_nf} + 1)/2) * ({pi_w} / {pi_nf} + 0.29)'
+ ps='2*int(({pi_nf} + 2)/2) * ({pi_w} / {pi_nf} + 0.29)' nrd='0.29 / {pi_w} ' nrs='0.29 / {pi_w} ' sa=0
+ sb=0 sd=0 mult=1 m=1
XM56 net36 pcas net49 VDPWR sky130_fd_pr__pfet_01v8 L={pic_l} W={pic_w} nf={pic_nf} ad='int(({pic_nf} + 1)/2) * {pic_w} / {pic_nf} * 0.29'
+ as='int(({pic_nf} + 2)/2) * {pic_w} / {pic_nf} * 0.29' pd='2*int(({pic_nf} + 1)/2) * ({pic_w} / {pic_nf} + 0.29)'
+ ps='2*int(({pic_nf} + 2)/2) * ({pic_w} / {pic_nf} + 0.29)' nrd='0.29 / {pic_w} ' nrs='0.29 / {pic_w} '
+ sa=0 sb=0 sd=0 mult=1 m=1
XM82 net50 net51 net25 VDPWR sky130_fd_pr__pfet_01v8 L={pi_l} W={pi_w} nf={pi_nf} ad='int(({pi_nf} + 1)/2) * {pi_w} / {pi_nf} * 0.29'
+ as='int(({pi_nf} + 2)/2) * {pi_w} / {pi_nf} * 0.29' pd='2*int(({pi_nf} + 1)/2) * ({pi_w} / {pi_nf} + 0.29)'
+ ps='2*int(({pi_nf} + 2)/2) * ({pi_w} / {pi_nf} + 0.29)' nrd='0.29 / {pi_w} ' nrs='0.29 / {pi_w} ' sa=0
+ sb=0 sd=0 mult=1 m=1
XM83 net51 pcas net50 VDPWR sky130_fd_pr__pfet_01v8 L={pic_l} W={pic_w} nf={pic_nf} ad='int(({pic_nf} + 1)/2) * {pic_w} / {pic_nf} * 0.29'
+ as='int(({pic_nf} + 2)/2) * {pic_w} / {pic_nf} * 0.29' pd='2*int(({pic_nf} + 1)/2) * ({pic_w} / {pic_nf} + 0.29)'
+ ps='2*int(({pic_nf} + 2)/2) * ({pic_w} / {pic_nf} + 0.29)' nrd='0.29 / {pic_w} ' nrs='0.29 / {pic_w} '
+ sa=0 sb=0 sd=0 mult=1 m=1
XC6 net3 pb sky130_fd_pr__cap_mim_m3_1 W={cd_l} L={cd_l} MF={cd_m} m={cd_m}
XC7 net3 pcas sky130_fd_pr__cap_mim_m3_1 W={cd_l} L={cd_l} MF={cd_m} m={cd_m}
XC8 nb VGND sky130_fd_pr__cap_mim_m3_1 W={cd_l} L={cd_l} MF={cd_m} m={cd_m}
XC9 ncas VGND sky130_fd_pr__cap_mim_m3_1 W={cd_l} L={cd_l} MF={cd_m} m={cd_m}
XC4 net36 pinm sky130_fd_pr__cap_mim_m3_1 W={cm1_l} L={cm1_l} MF=1 m=1
XM5 net40 midm net55 VDPWR sky130_fd_pr__pfet_01v8_lvt L={poi_l} W={poi_w} nf={poi_nf} ad='int(({poi_nf} + 1)/2) * {poi_w} / {poi_nf} * 0.29'
+ as='int(({poi_nf} + 2)/2) * {poi_w} / {poi_nf} * 0.29' pd='2*int(({poi_nf} + 1)/2) * ({poi_w} / {poi_nf} + 0.29)'
+ ps='2*int(({poi_nf} + 2)/2) * ({poi_w} / {poi_nf} + 0.29)' nrd='0.29 / {poi_w} ' nrs='0.29 / {poi_w} '
+ sa=0 sb=0 sd=0 mult=2 m=2
XM62 net40 ncas net52 VGND sky130_fd_pr__nfet_01v8 L={nic_l} W={nic_w} nf={nic_nf} ad='int(({nic_nf} + 1)/2) * {nic_w} / {nic_nf} * 0.29'
+ as='int(({nic_nf} + 2)/2) * {nic_w} / {nic_nf} * 0.29' pd='2*int(({nic_nf} + 1)/2) * ({nic_w} / {nic_nf} + 0.29)'
+ ps='2*int(({nic_nf} + 2)/2) * ({nic_w} / {nic_nf} + 0.29)' nrd='0.29 / {nic_w} ' nrs='0.29 / {nic_w} '
+ sa=0 sb=0 sd=0 mult={s2_m} m={s2_m}
XM84 net52 net54 VGND VGND sky130_fd_pr__nfet_01v8 L={ni_l} W={ni_w} nf={ni_nf} ad='int(({ni_nf} + 1)/2) * {ni_w} / {ni_nf} * 0.29'
+ as='int(({ni_nf} + 2)/2) * {ni_w} / {ni_nf} * 0.29' pd='2*int(({ni_nf} + 1)/2) * ({ni_w} / {ni_nf} + 0.29)'
+ ps='2*int(({ni_nf} + 2)/2) * ({ni_w} / {ni_nf} + 0.29)' nrd='0.29 / {ni_w} ' nrs='0.29 / {ni_w} ' sa=0
+ sb=0 sd=0 mult={s2_m} m={s2_m}
XM87 net54 ncas net53 VGND sky130_fd_pr__nfet_01v8 L={nic_l} W={nic_w} nf={nic_nf} ad='int(({nic_nf} + 1)/2) * {nic_w} / {nic_nf} * 0.29'
+ as='int(({nic_nf} + 2)/2) * {nic_w} / {nic_nf} * 0.29' pd='2*int(({nic_nf} + 1)/2) * ({nic_w} / {nic_nf} + 0.29)'
+ ps='2*int(({nic_nf} + 2)/2) * ({nic_w} / {nic_nf} + 0.29)' nrd='0.29 / {nic_w} ' nrs='0.29 / {nic_w} '
+ sa=0 sb=0 sd=0 mult={s2_m} m={s2_m}
XM88 net53 net54 VGND VGND sky130_fd_pr__nfet_01v8 L={ni_l} W={ni_w} nf={ni_nf} ad='int(({ni_nf} + 1)/2) * {ni_w} / {ni_nf} * 0.29'
+ as='int(({ni_nf} + 2)/2) * {ni_w} / {ni_nf} * 0.29' pd='2*int(({ni_nf} + 1)/2) * ({ni_w} / {ni_nf} + 0.29)'
+ ps='2*int(({ni_nf} + 2)/2) * ({ni_w} / {ni_nf} + 0.29)' nrd='0.29 / {ni_w} ' nrs='0.29 / {ni_w} ' sa=0
+ sb=0 sd=0 mult={s2_m} m={s2_m}
XM89 net56 pb net37 VDPWR sky130_fd_pr__pfet_01v8 L={pi_l} W={pi_w} nf={pi_nf} ad='int(({pi_nf} + 1)/2) * {pi_w} / {pi_nf} * 0.29'
+ as='int(({pi_nf} + 2)/2) * {pi_w} / {pi_nf} * 0.29' pd='2*int(({pi_nf} + 1)/2) * ({pi_w} / {pi_nf} + 0.29)'
+ ps='2*int(({pi_nf} + 2)/2) * ({pi_w} / {pi_nf} + 0.29)' nrd='0.29 / {pi_w} ' nrs='0.29 / {pi_w} ' sa=0
+ sb=0 sd=0 mult={s2_m} m={s2_m}
XM90 net55 pcas net56 VDPWR sky130_fd_pr__pfet_01v8 L={pic_l} W={pic_w} nf={pic_nf} ad='int(({pic_nf} + 1)/2) * {pic_w} / {pic_nf} * 0.29'
+ as='int(({pic_nf} + 2)/2) * {pic_w} / {pic_nf} * 0.29' pd='2*int(({pic_nf} + 1)/2) * ({pic_w} / {pic_nf} + 0.29)'
+ ps='2*int(({pic_nf} + 2)/2) * ({pic_w} / {pic_nf} + 0.29)' nrd='0.29 / {pic_w} ' nrs='0.29 / {pic_w} '
+ sa=0 sb=0 sd=0 mult={s2_m} m={s2_m}
XM91 net40 ncas net57 VGND sky130_fd_pr__nfet_01v8 L={nic_l} W={nic_w} nf={nic_nf} ad='int(({nic_nf} + 1)/2) * {nic_w} / {nic_nf} * 0.29'
+ as='int(({nic_nf} + 2)/2) * {nic_w} / {nic_nf} * 0.29' pd='2*int(({nic_nf} + 1)/2) * ({nic_w} / {nic_nf} + 0.29)'
+ ps='2*int(({nic_nf} + 2)/2) * ({nic_w} / {nic_nf} + 0.29)' nrd='0.29 / {nic_w} ' nrs='0.29 / {nic_w} '
+ sa=0 sb=0 sd=0 mult={io_m} m={io_m}
XM92 net57 nb VGND VGND sky130_fd_pr__nfet_01v8 L={ni_l} W={ni_w} nf={ni_nf} ad='int(({ni_nf} + 1)/2) * {ni_w} / {ni_nf} * 0.29'
+ as='int(({ni_nf} + 2)/2) * {ni_w} / {ni_nf} * 0.29' pd='2*int(({ni_nf} + 1)/2) * ({ni_w} / {ni_nf} + 0.29)'
+ ps='2*int(({ni_nf} + 2)/2) * ({ni_w} / {ni_nf} + 0.29)' nrd='0.29 / {ni_w} ' nrs='0.29 / {ni_w} ' sa=0
+ sb=0 sd=0 mult={io_m} m={io_m}
XC1 net58 midp sky130_fd_pr__cap_mim_m3_1 W={c_l} L={c_l} MF=1 m=1
XC2 net59 net41 sky130_fd_pr__cap_mim_m3_1 W={c2_l} L={c2_l} MF=1 m=1
XC3 net60 net40 sky130_fd_pr__cap_mim_m3_1 W={c2_l} L={c2_l} MF=1 m=1
XR1 out net58 VGND sky130_fd_pr__res_xhigh_po_1p41 L={rc_l} mult=1 m=1
XR2 net58 net59 VGND sky130_fd_pr__res_xhigh_po_1p41 L={rc2_l} mult=1 m=1
XR3 net58 net60 VGND sky130_fd_pr__res_xhigh_po_1p41 L={rc2_l} mult=1 m=1
Vmidn midp net62 0
.save i(vmidn)
Vmidp net61 midp 0
.save i(vmidp)
**.ends

* expanding   symbol:  /foss/designs/ttsky26c-analog-park/xschem/bias.sym # of pins=5
** sym_path: xschem/bias.sym
** sch_path: xschem/bias.sch
.subckt bias VDPWR pIout VGND EN vbias
*.ipin EN
*.opin pIout
*.ipin VGND
*.ipin VDPWR
*.opin vbias
XM4 inm vbias VDPWR VDPWR sky130_fd_pr__pfet_01v8_lvt L=2 W=2 nf=1 ad='int((1 + 1)/2) * 2 / 1 * 0.29'
+ as='int((1 + 2)/2) * 2 / 1 * 0.29' pd='2*int((1 + 1)/2) * (2 / 1 + 0.29)' ps='2*int((1 + 2)/2) * (2 / 1 + 0.29)'
+ nrd='0.29 / 2 ' nrs='0.29 / 2 ' sa=0 sb=0 sd=0 mult=2 m=2
XM2 inp vbias VDPWR VDPWR sky130_fd_pr__pfet_01v8_lvt L=2 W=2 nf=1 ad='int((1 + 1)/2) * 2 / 1 * 0.29'
+ as='int((1 + 2)/2) * 2 / 1 * 0.29' pd='2*int((1 + 1)/2) * (2 / 1 + 0.29)' ps='2*int((1 + 2)/2) * (2 / 1 + 0.29)'
+ nrd='0.29 / 2 ' nrs='0.29 / 2 ' sa=0 sb=0 sd=0 mult=2 m=2
XM5 pIout vbias VDPWR VDPWR sky130_fd_pr__pfet_01v8_lvt L=2 W=2 nf=1 ad='int((1 + 1)/2) * 2 / 1 * 0.29'
+ as='int((1 + 2)/2) * 2 / 1 * 0.29' pd='2*int((1 + 1)/2) * (2 / 1 + 0.29)' ps='2*int((1 + 2)/2) * (2 / 1 + 0.29)'
+ nrd='0.29 / 2 ' nrs='0.29 / 2 ' sa=0 sb=0 sd=0 mult=2 m=2
XM8 inm inm VGND VGND sky130_fd_pr__nfet_01v8 L=2 W=4 nf=1 ad='int((1 + 1)/2) * 4 / 1 * 0.29' as='int((1 + 2)/2) * 4 / 1 * 0.29'
+ pd='2*int((1 + 1)/2) * (4 / 1 + 0.29)' ps='2*int((1 + 2)/2) * (4 / 1 + 0.29)' nrd='0.29 / 4 ' nrs='0.29 / 4 '
+ sa=0 sb=0 sd=0 mult=1 m=1
XM9 inp inp net1 VGND sky130_fd_pr__nfet_01v8 L=2 W=4 nf=1 ad='int((1 + 1)/2) * 4 / 1 * 0.29' as='int((1 + 2)/2) * 4 / 1 * 0.29'
+ pd='2*int((1 + 1)/2) * (4 / 1 + 0.29)' ps='2*int((1 + 2)/2) * (4 / 1 + 0.29)' nrd='0.29 / 4 ' nrs='0.29 / 4 '
+ sa=0 sb=0 sd=0 mult=4 m=4
XM10 net2 inp VGND VGND sky130_fd_pr__nfet_01v8 L=2 W=2 nf=1 ad='int((1 + 1)/2) * 2 / 1 * 0.29' as='int((1 + 2)/2) * 2 / 1 * 0.29'
+ pd='2*int((1 + 1)/2) * (2 / 1 + 0.29)' ps='2*int((1 + 2)/2) * (2 / 1 + 0.29)' nrd='0.29 / 2 ' nrs='0.29 / 2 '
+ sa=0 sb=0 sd=0 mult=2 m=2
XM11 vbias inm VGND VGND sky130_fd_pr__nfet_01v8 L=2 W=2 nf=1 ad='int((1 + 1)/2) * 2 / 1 * 0.29' as='int((1 + 2)/2) * 2 / 1 * 0.29'
+ pd='2*int((1 + 1)/2) * (2 / 1 + 0.29)' ps='2*int((1 + 2)/2) * (2 / 1 + 0.29)' nrd='0.29 / 2 ' nrs='0.29 / 2 '
+ sa=0 sb=0 sd=0 mult=2 m=2
XM15 vbias startup inm VGND sky130_fd_pr__nfet_01v8_lvt L=0.15 W=0.5 nf=1 ad='int((1 + 1)/2) * 0.5 / 1 * 0.29'
+ as='int((1 + 2)/2) * 0.5 / 1 * 0.29' pd='2*int((1 + 1)/2) * (0.5 / 1 + 0.29)' ps='2*int((1 + 2)/2) * (0.5 / 1 + 0.29)'
+ nrd='0.29 / 0.5 ' nrs='0.29 / 0.5 ' sa=0 sb=0 sd=0 mult=1 m=1
XM3 startup inm VGND VGND sky130_fd_pr__nfet_01v8 L=0.5 W=0.5 nf=1 ad='int((1 + 1)/2) * 0.5 / 1 * 0.29'
+ as='int((1 + 2)/2) * 0.5 / 1 * 0.29' pd='2*int((1 + 1)/2) * (0.5 / 1 + 0.29)' ps='2*int((1 + 2)/2) * (0.5 / 1 + 0.29)'
+ nrd='0.29 / 0.5 ' nrs='0.29 / 0.5 ' sa=0 sb=0 sd=0 mult=1 m=1
XR1 net4 net1 VGND sky130_fd_pr__res_high_po_0p69 L=6.1 mult=1 m=1
XR2 net5 net4 VGND sky130_fd_pr__res_high_po_0p69 L=6.1 mult=1 m=1
XR3 net6 net5 VGND sky130_fd_pr__res_high_po_0p69 L=6.1 mult=1 m=1
XR4 VGND net6 VGND sky130_fd_pr__res_high_po_0p69 L=6.1 mult=1 m=1
XM1 vbias net2 VDPWR VDPWR sky130_fd_pr__pfet_01v8_lvt L=2 W=2 nf=1 ad='int((1 + 1)/2) * 2 / 1 * 0.29'
+ as='int((1 + 2)/2) * 2 / 1 * 0.29' pd='2*int((1 + 1)/2) * (2 / 1 + 0.29)' ps='2*int((1 + 2)/2) * (2 / 1 + 0.29)'
+ nrd='0.29 / 2 ' nrs='0.29 / 2 ' sa=0 sb=0 sd=0 mult=2 m=2
XM12 net2 net2 VDPWR VDPWR sky130_fd_pr__pfet_01v8_lvt L=2 W=2 nf=1 ad='int((1 + 1)/2) * 2 / 1 * 0.29'
+ as='int((1 + 2)/2) * 2 / 1 * 0.29' pd='2*int((1 + 1)/2) * (2 / 1 + 0.29)' ps='2*int((1 + 2)/2) * (2 / 1 + 0.29)'
+ nrd='0.29 / 2 ' nrs='0.29 / 2 ' sa=0 sb=0 sd=0 mult=2 m=2
XM13 startup startup net3 VDPWR sky130_fd_pr__pfet_01v8_lvt L=3 W=0.42 nf=1 ad='int((1 + 1)/2) * 0.42 / 1 * 0.29'
+ as='int((1 + 2)/2) * 0.42 / 1 * 0.29' pd='2*int((1 + 1)/2) * (0.42 / 1 + 0.29)' ps='2*int((1 + 2)/2) * (0.42 / 1 + 0.29)'
+ nrd='0.29 / 0.42 ' nrs='0.29 / 0.42 ' sa=0 sb=0 sd=0 mult=1 m=1
XM16 startup nEN VGND VGND sky130_fd_pr__nfet_01v8 L=0.15 W=0.5 nf=1 ad='int((1 + 1)/2) * 0.5 / 1 * 0.29'
+ as='int((1 + 2)/2) * 0.5 / 1 * 0.29' pd='2*int((1 + 1)/2) * (0.5 / 1 + 0.29)' ps='2*int((1 + 2)/2) * (0.5 / 1 + 0.29)'
+ nrd='0.29 / 0.5 ' nrs='0.29 / 0.5 ' sa=0 sb=0 sd=0 mult=1 m=1
XM17 vbias EN VDPWR VDPWR sky130_fd_pr__pfet_01v8_hvt L=0.15 W=0.42 nf=1 ad='int((1 + 1)/2) * 0.42 / 1 * 0.29'
+ as='int((1 + 2)/2) * 0.42 / 1 * 0.29' pd='2*int((1 + 1)/2) * (0.42 / 1 + 0.29)' ps='2*int((1 + 2)/2) * (0.42 / 1 + 0.29)'
+ nrd='0.29 / 0.42 ' nrs='0.29 / 0.42 ' sa=0 sb=0 sd=0 mult=1 m=1
XM7 net3 nEN VDPWR VDPWR sky130_fd_pr__pfet_01v8_hvt L=0.15 W=0.42 nf=1 ad='int((1 + 1)/2) * 0.42 / 1 * 0.29'
+ as='int((1 + 2)/2) * 0.42 / 1 * 0.29' pd='2*int((1 + 1)/2) * (0.42 / 1 + 0.29)' ps='2*int((1 + 2)/2) * (0.42 / 1 + 0.29)'
+ nrd='0.29 / 0.42 ' nrs='0.29 / 0.42 ' sa=0 sb=0 sd=0 mult=1 m=1
XM14 VDPWR vbias VDPWR VDPWR sky130_fd_pr__pfet_01v8_lvt L=3 W=4 nf=1 ad='int((1 + 1)/2) * 4 / 1 * 0.29'
+ as='int((1 + 2)/2) * 4 / 1 * 0.29' pd='2*int((1 + 1)/2) * (4 / 1 + 0.29)' ps='2*int((1 + 2)/2) * (4 / 1 + 0.29)'
+ nrd='0.29 / 4 ' nrs='0.29 / 4 ' sa=0 sb=0 sd=0 mult=6 m=6
x1 EN VGND VGND VDPWR VDPWR nEN sky130_fd_sc_hd__inv_1
.ends

.end
